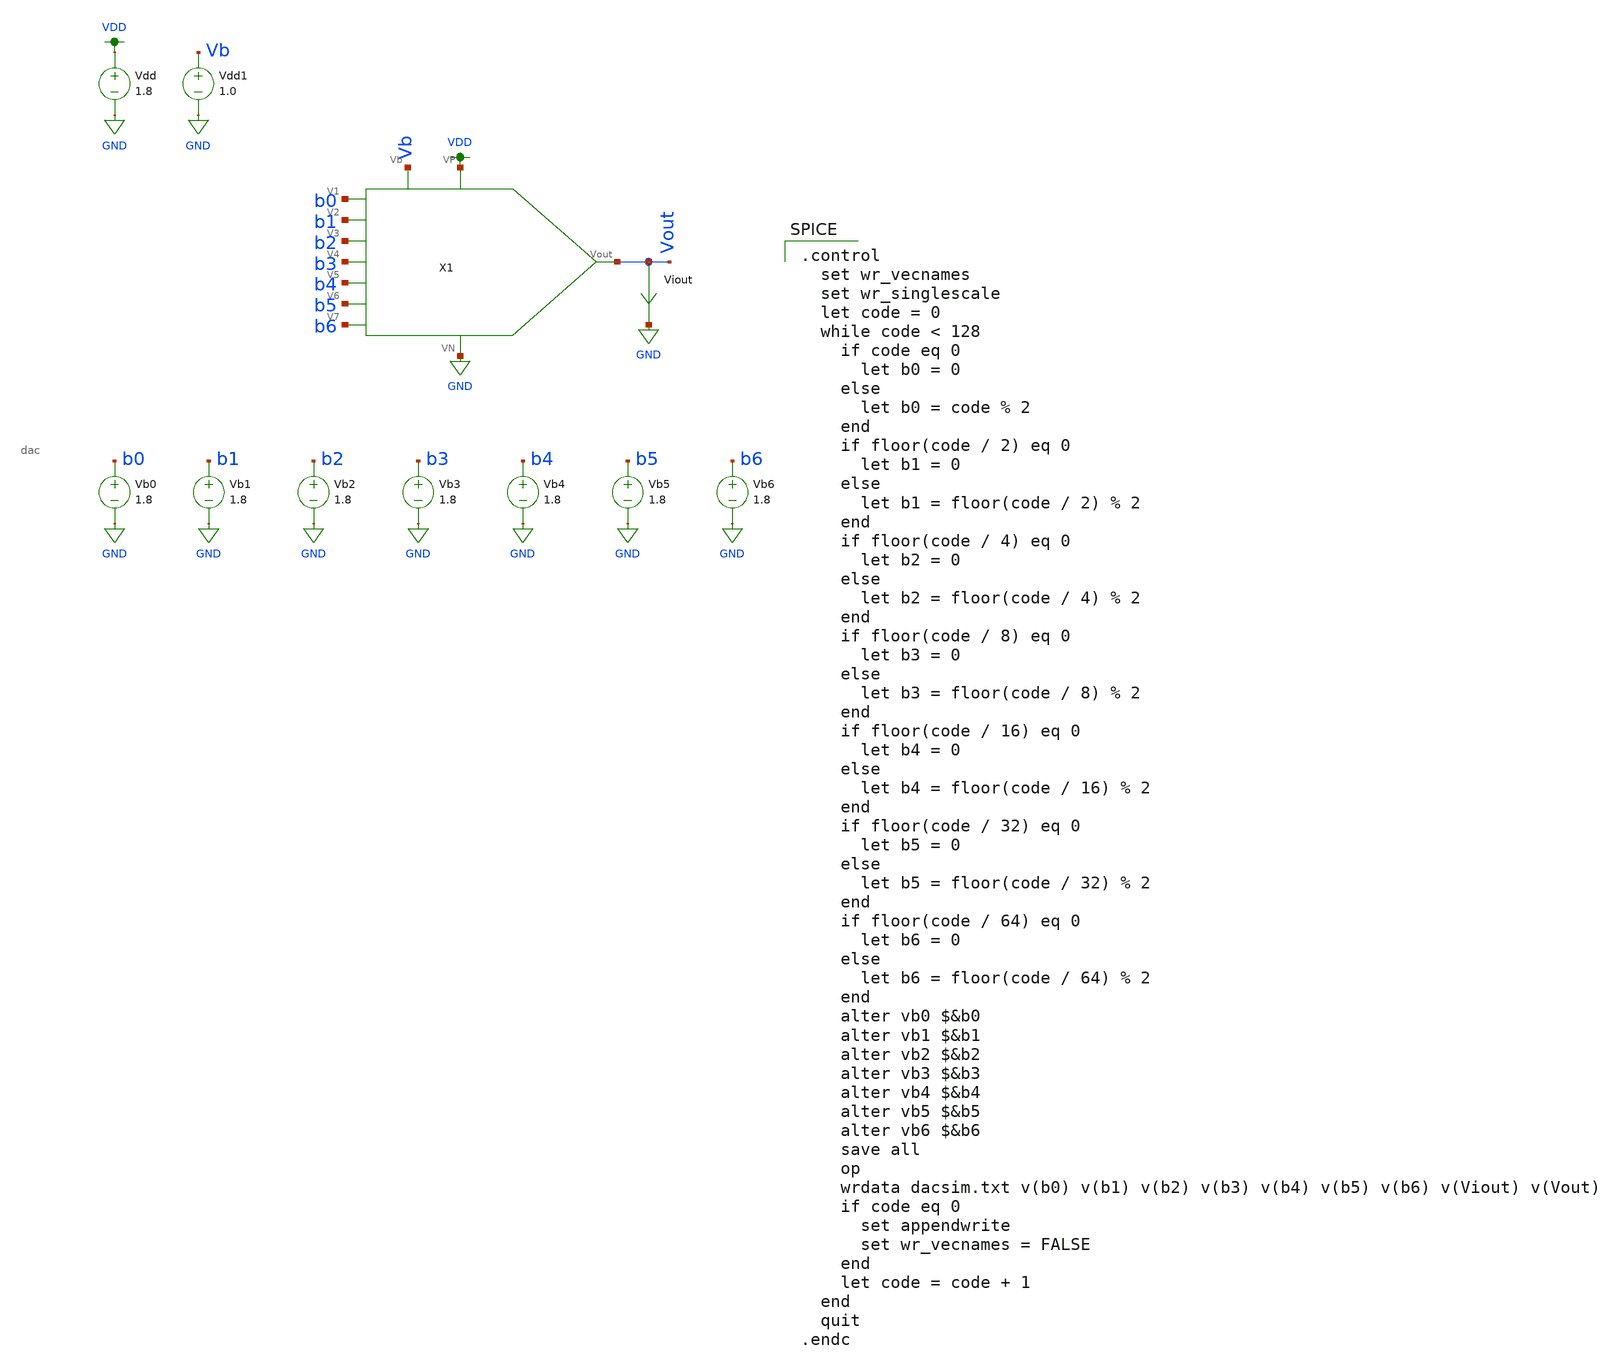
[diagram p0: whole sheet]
** sch_path: schematics/dac_sim.sch
**.subckt dac_sim
Vdd VDD GND 1.8
Viout Vout GND 0
.save i(viout)
Vb0 b0 GND 1.8
Vdd1 Vb GND 1.0
Vb1 b1 GND 1.8
Vb2 b2 GND 1.8
Vb3 b3 GND 1.8
Vb4 b4 GND 1.8
Vb5 b5 GND 1.8
Vb6 b6 GND 1.8
X1 b0 b1 b2 b3 b4 b5 b6 Vout VDD GND Vb dac
**** begin user architecture code

.option wnflag=1
.param MC_SWITCH=1.0
.lib ~/skywater/skywater-pdk/libraries/sky130_fd_pr_ngspice/latest/models/sky130.lib.spice tt


.control
  set wr_vecnames
  set wr_singlescale
  let code = 0
  while code < 128
    if code eq 0
      let b0 = 0
    else
      let b0 = code % 2
    end
    if floor(code / 2) eq 0
      let b1 = 0
    else
      let b1 = floor(code / 2) % 2
    end
    if floor(code / 4) eq 0
      let b2 = 0
    else
      let b2 = floor(code / 4) % 2
    end
    if floor(code / 8) eq 0
      let b3 = 0
    else
      let b3 = floor(code / 8) % 2
    end
    if floor(code / 16) eq 0
      let b4 = 0
    else
      let b4 = floor(code / 16) % 2
    end
    if floor(code / 32) eq 0
      let b5 = 0
    else
      let b5 = floor(code / 32) % 2
    end
    if floor(code / 64) eq 0
      let b6 = 0
    else
      let b6 = floor(code / 64) % 2
    end
    alter vb0 $&b0
    alter vb1 $&b1
    alter vb2 $&b2
    alter vb3 $&b3
    alter vb4 $&b4
    alter vb5 $&b5
    alter vb6 $&b6
    save all
    op
    wrdata dacsim.txt v(b0) v(b1) v(b2) v(b3) v(b4) v(b5) v(b6) v(Viout) v(Vout)
    if code eq 0
      set appendwrite
      set wr_vecnames = FALSE
    end
    let code = code + 1
  end
  quit
.endc

**** end user architecture code
**.ends

* expanding   symbol:  /home/madvlsi/Documents/current-output-dac-vlsi/schematics/dac.sym # of
*+ pins=11
** sym_path: schematics/dac.sym
** sch_path: schematics/dac.sch
.subckt dac V1 V2 V3 V4 V5 V6 V7 Vout VP VN Vb
*.iopin VN
*.iopin VP
*.ipin V1
*.ipin V2
*.ipin V3
*.ipin V4
*.ipin V5
*.ipin V6
*.ipin V7
*.ipin Vb
*.opin Vout
XM1 V1 Vb Vout VDD sky130_fd_pr__pfet_01v8 L=0.15 W=1 nf=1 ad='int((nf+1)/2) * W/nf * 0.29' as='int((nf+2)/2) * W/nf * 0.29'
+ pd='2*int((nf+1)/2) * (W/nf + 0.29)' ps='2*int((nf+2)/2) * (W/nf + 0.29)' nrd='0.29 / W' nrs='0.29 / W'
+ sa=0 sb=0 sd=0 mult=1 m=1
XM2 net1 Vb Vout VDD sky130_fd_pr__pfet_01v8 L=0.15 W=1 nf=1 ad='int((nf+1)/2) * W/nf * 0.29' as='int((nf+2)/2) * W/nf * 0.29'
+ pd='2*int((nf+1)/2) * (W/nf + 0.29)' ps='2*int((nf+2)/2) * (W/nf + 0.29)' nrd='0.29 / W' nrs='0.29 / W'
+ sa=0 sb=0 sd=0 mult=1 m=1
XM3 V2 Vb net1 VDD sky130_fd_pr__pfet_01v8 L=0.15 W=1 nf=1 ad='int((nf+1)/2) * W/nf * 0.29' as='int((nf+2)/2) * W/nf * 0.29'
+ pd='2*int((nf+1)/2) * (W/nf + 0.29)' ps='2*int((nf+2)/2) * (W/nf + 0.29)' nrd='0.29 / W' nrs='0.29 / W'
+ sa=0 sb=0 sd=0 mult=1 m=1
XM4 net2 Vb net1 VDD sky130_fd_pr__pfet_01v8 L=0.15 W=1 nf=1 ad='int((nf+1)/2) * W/nf * 0.29' as='int((nf+2)/2) * W/nf * 0.29'
+ pd='2*int((nf+1)/2) * (W/nf + 0.29)' ps='2*int((nf+2)/2) * (W/nf + 0.29)' nrd='0.29 / W' nrs='0.29 / W'
+ sa=0 sb=0 sd=0 mult=1 m=1
XM5 V3 Vb net2 VDD sky130_fd_pr__pfet_01v8 L=0.15 W=1 nf=1 ad='int((nf+1)/2) * W/nf * 0.29' as='int((nf+2)/2) * W/nf * 0.29'
+ pd='2*int((nf+1)/2) * (W/nf + 0.29)' ps='2*int((nf+2)/2) * (W/nf + 0.29)' nrd='0.29 / W' nrs='0.29 / W'
+ sa=0 sb=0 sd=0 mult=1 m=1
XM6 net3 Vb net2 VDD sky130_fd_pr__pfet_01v8 L=0.15 W=1 nf=1 ad='int((nf+1)/2) * W/nf * 0.29' as='int((nf+2)/2) * W/nf * 0.29'
+ pd='2*int((nf+1)/2) * (W/nf + 0.29)' ps='2*int((nf+2)/2) * (W/nf + 0.29)' nrd='0.29 / W' nrs='0.29 / W'
+ sa=0 sb=0 sd=0 mult=1 m=1
XM7 V4 Vb net3 VDD sky130_fd_pr__pfet_01v8 L=0.15 W=1 nf=1 ad='int((nf+1)/2) * W/nf * 0.29' as='int((nf+2)/2) * W/nf * 0.29'
+ pd='2*int((nf+1)/2) * (W/nf + 0.29)' ps='2*int((nf+2)/2) * (W/nf + 0.29)' nrd='0.29 / W' nrs='0.29 / W'
+ sa=0 sb=0 sd=0 mult=1 m=1
XM8 net4 Vb net3 VDD sky130_fd_pr__pfet_01v8 L=0.15 W=1 nf=1 ad='int((nf+1)/2) * W/nf * 0.29' as='int((nf+2)/2) * W/nf * 0.29'
+ pd='2*int((nf+1)/2) * (W/nf + 0.29)' ps='2*int((nf+2)/2) * (W/nf + 0.29)' nrd='0.29 / W' nrs='0.29 / W'
+ sa=0 sb=0 sd=0 mult=1 m=1
XM9 V5 Vb net4 VDD sky130_fd_pr__pfet_01v8 L=0.15 W=1 nf=1 ad='int((nf+1)/2) * W/nf * 0.29' as='int((nf+2)/2) * W/nf * 0.29'
+ pd='2*int((nf+1)/2) * (W/nf + 0.29)' ps='2*int((nf+2)/2) * (W/nf + 0.29)' nrd='0.29 / W' nrs='0.29 / W'
+ sa=0 sb=0 sd=0 mult=1 m=1
XM10 net5 Vb net4 VDD sky130_fd_pr__pfet_01v8 L=0.15 W=1 nf=1 ad='int((nf+1)/2) * W/nf * 0.29' as='int((nf+2)/2) * W/nf * 0.29'
+ pd='2*int((nf+1)/2) * (W/nf + 0.29)' ps='2*int((nf+2)/2) * (W/nf + 0.29)' nrd='0.29 / W' nrs='0.29 / W'
+ sa=0 sb=0 sd=0 mult=1 m=1
XM11 V6 Vb net5 VDD sky130_fd_pr__pfet_01v8 L=0.15 W=1 nf=1 ad='int((nf+1)/2) * W/nf * 0.29' as='int((nf+2)/2) * W/nf * 0.29'
+ pd='2*int((nf+1)/2) * (W/nf + 0.29)' ps='2*int((nf+2)/2) * (W/nf + 0.29)' nrd='0.29 / W' nrs='0.29 / W'
+ sa=0 sb=0 sd=0 mult=1 m=1
XM12 net6 Vb net5 VDD sky130_fd_pr__pfet_01v8 L=0.15 W=1 nf=1 ad='int((nf+1)/2) * W/nf * 0.29' as='int((nf+2)/2) * W/nf * 0.29'
+ pd='2*int((nf+1)/2) * (W/nf + 0.29)' ps='2*int((nf+2)/2) * (W/nf + 0.29)' nrd='0.29 / W' nrs='0.29 / W'
+ sa=0 sb=0 sd=0 mult=1 m=1
XM13 V7 Vb net6 VDD sky130_fd_pr__pfet_01v8 L=0.15 W=1 nf=1 ad='int((nf+1)/2) * W/nf * 0.29' as='int((nf+2)/2) * W/nf * 0.29'
+ pd='2*int((nf+1)/2) * (W/nf + 0.29)' ps='2*int((nf+2)/2) * (W/nf + 0.29)' nrd='0.29 / W' nrs='0.29 / W'
+ sa=0 sb=0 sd=0 mult=1 m=1
XM14 VN Vb net6 VDD sky130_fd_pr__pfet_01v8 L=0.15 W=1 nf=1 ad='int((nf+1)/2) * W/nf * 0.29' as='int((nf+2)/2) * W/nf * 0.29'
+ pd='2*int((nf+1)/2) * (W/nf + 0.29)' ps='2*int((nf+2)/2) * (W/nf + 0.29)' nrd='0.29 / W' nrs='0.29 / W'
+ sa=0 sb=0 sd=0 mult=1 m=1
XM15 VP Vb Vb VDD sky130_fd_pr__pfet_01v8 L=0.15 W=1 nf=1 ad='int((nf+1)/2) * W/nf * 0.29' as='int((nf+2)/2) * W/nf * 0.29'
+ pd='2*int((nf+1)/2) * (W/nf + 0.29)' ps='2*int((nf+2)/2) * (W/nf + 0.29)' nrd='0.29 / W' nrs='0.29 / W'
+ sa=0 sb=0 sd=0 mult=1 m=1
.ends

.GLOBAL GND
.GLOBAL VDD
.end
